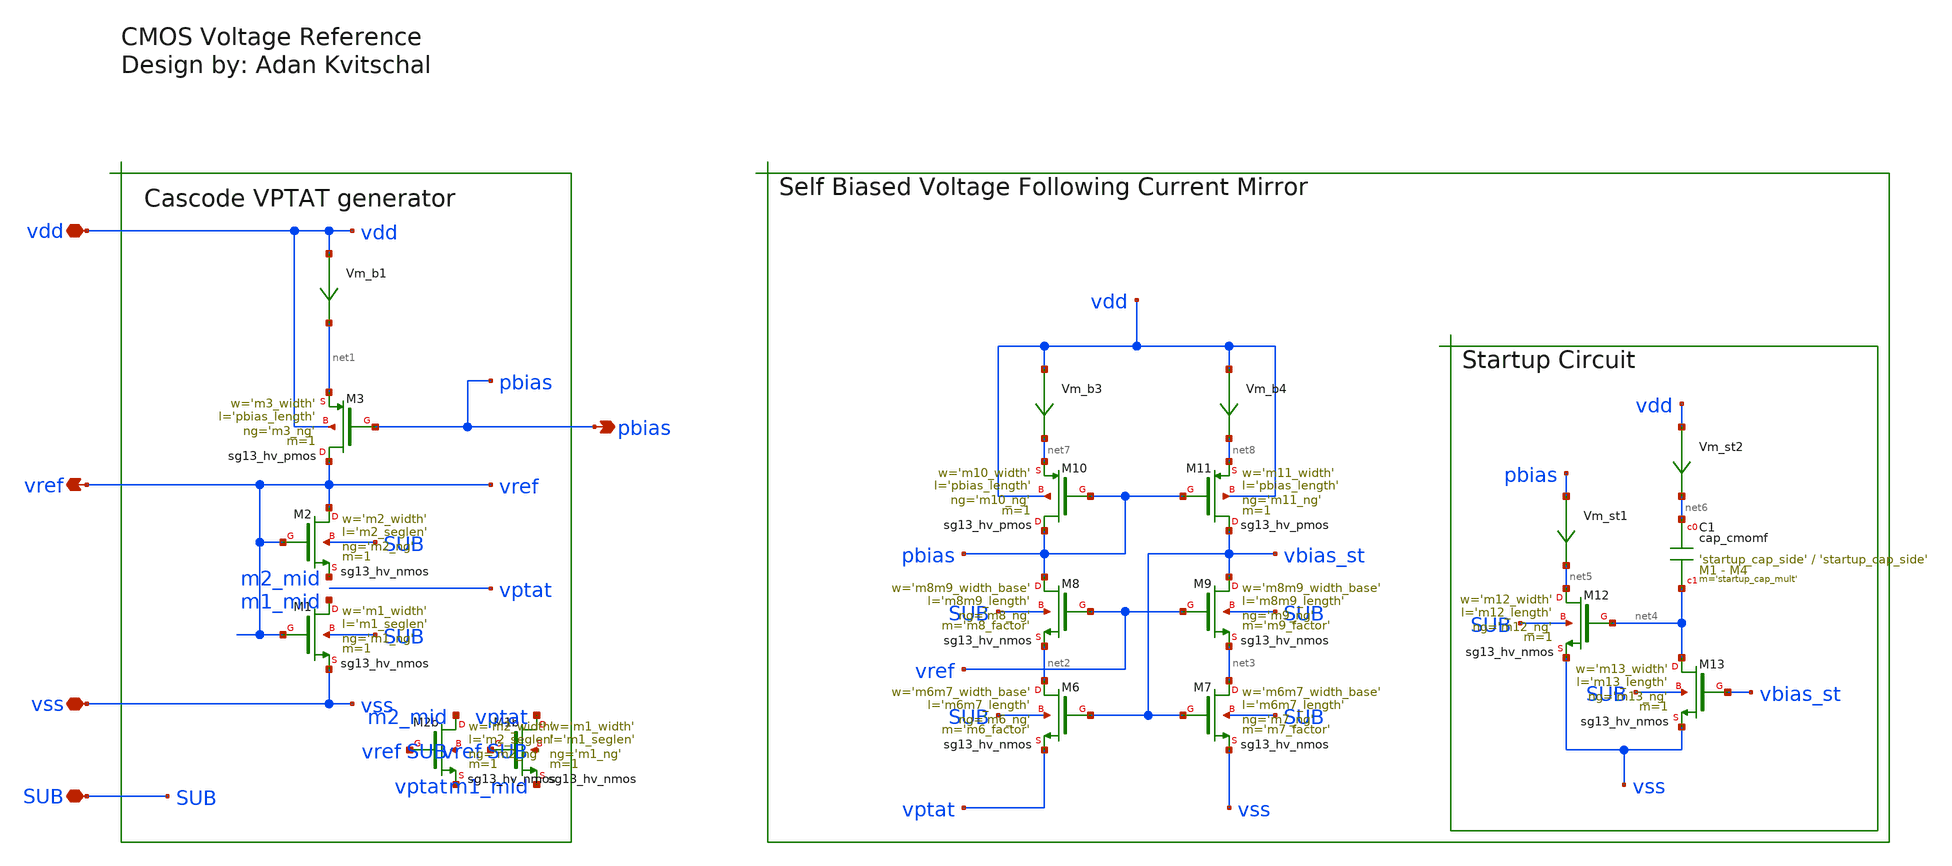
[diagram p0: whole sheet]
** sch_path: sch/cmos_vref/cmos_vref_default.sch
**.subckt cmos_vref_default vss SUB vdd pbias vref
*.iopin vss
*.iopin SUB
*.iopin vdd
*.opin pbias
*.opin vref
Vm_b1 vdd net1 0
.save i(vm_b1)
XM1 m1_mid vref vss SUB sg13_hv_nmos w='m1_width' l='m1_seglen' ng='m1_ng' m=1 mm_ok=1
XM2 vref vref m2_mid SUB sg13_hv_nmos w='m2_width' l='m2_seglen' ng='m2_ng' m=1 mm_ok=1
XM3 vref pbias net1 vdd sg13_hv_pmos w='m3_width' l='pbias_length' ng='m3_ng' m=1 mm_ok=1
Vm_st1 pbias net5 0
.save i(vm_st1)
Vm_st2 vdd net6 0
.save i(vm_st2)
Vm_b3 vdd net7 0
.save i(vm_b3)
Vm_b4 vdd net8 0
.save i(vm_b4)
XM7 net3 vbias_st vss SUB sg13_hv_nmos w='m6m7_width_base' l='m6m7_length' ng='m7_ng' m='m7_factor' mm_ok=1
XM11 vbias_st pbias net8 vdd sg13_hv_pmos w='m11_width' l='pbias_length' ng='m11_ng' m=1 mm_ok=1
XM6 net2 vbias_st vptat SUB sg13_hv_nmos w='m6m7_width_base' l='m6m7_length' ng='m6_ng' m='m6_factor'
+ mm_ok=1
XM9 vbias_st vref net3 SUB sg13_hv_nmos w='m8m9_width_base' l='m8m9_length' ng='m9_ng' m='m9_factor'
+ mm_ok=1
XM8 pbias vref net2 SUB sg13_hv_nmos w='m8m9_width_base' l='m8m9_length' ng='m8_ng' m='m8_factor' mm_ok=1
XM10 pbias pbias net7 vdd sg13_hv_pmos w='m10_width' l='pbias_length' ng='m10_ng' m=1 mm_ok=1
XM13 net4 vbias_st vss SUB sg13_hv_nmos w='m13_width' l='m13_length' ng='m13_ng' m=1 mm_ok=1
XM12 net5 net4 vss SUB sg13_hv_nmos w='m12_width' l='m12_length' ng='m12_ng' m=1 mm_ok=1
XC1 net6 net4 cap_cmomf w='startup_cap_side' l='startup_cap_side' mmin=1 mmax=4 subblock=0 rfmodel=0
+ subscale=1 m='startup_cap_mult' mm_ok=1
XM1b vptat vref m1_mid SUB sg13_hv_nmos w='m1_width' l='m1_seglen' ng='m1_ng' m=1 mm_ok=1
XM2b m2_mid vref vptat SUB sg13_hv_nmos w='m2_width' l='m2_seglen' ng='m2_ng' m=1 mm_ok=1
**.ends
.end
